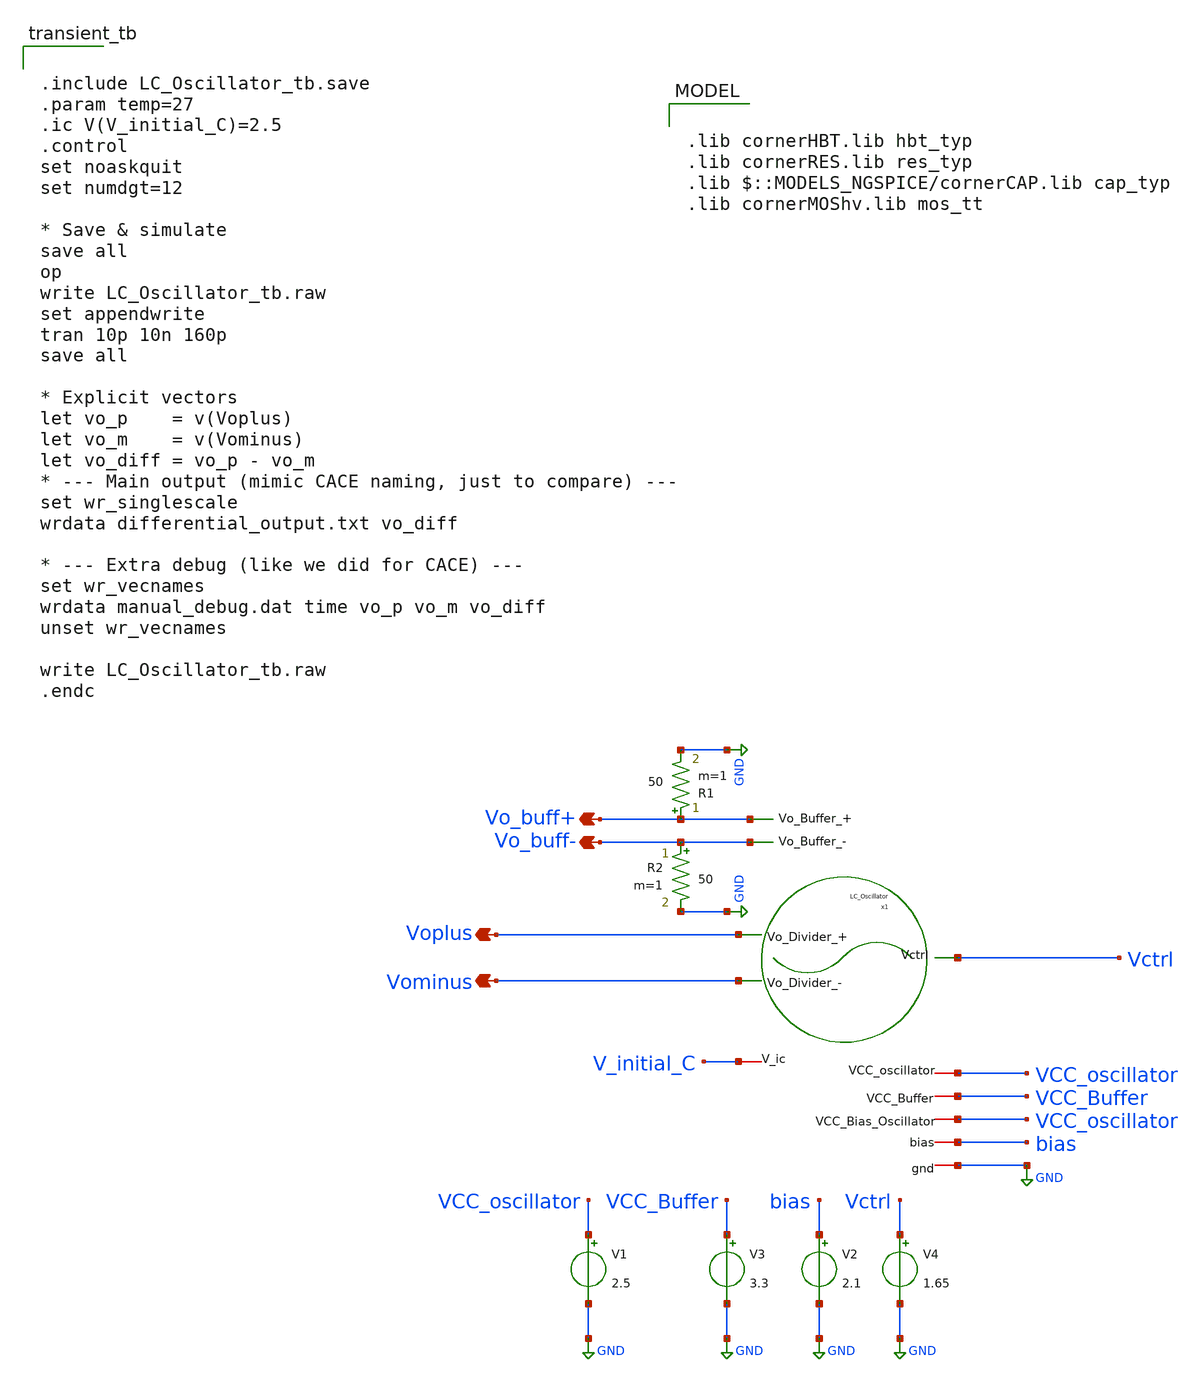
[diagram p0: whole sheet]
** sch_path: modules/module_4_type_2_PLL/LC_Oscillator/testbench/LC_Oscillator_tb.sch
**.subckt LC_Oscillator_tb Voplus Vominus Vo_buff+ Vo_buff-
*.opin Voplus
*.opin Vominus
*.opin Vo_buff+
*.opin Vo_buff-
V1 VCC_oscillator GND 2.5
x1 Voplus VCC_oscillator GND Vominus Vctrl bias VCC_Buffer VCC_oscillator Vo_buff- Vo_buff+
+ V_initial_C LC_Oscillator
V2 bias GND 2.1
V3 VCC_Buffer GND 3.3
R1 Vo_buff+ GND 50 m=1
R2 Vo_buff- GND 50 m=1
V4 Vctrl GND 1.65
**** begin user architecture code


.include LC_Oscillator_tb.save
.param temp=27
.ic V(V_initial_C)=2.5
.control
set noaskquit
set numdgt=12

* Save & simulate
save all
op
write LC_Oscillator_tb.raw
set appendwrite
tran 10p 10n 160p
save all

* Explicit vectors
let vo_p    = v(Voplus)
let vo_m    = v(Vominus)
let vo_diff = vo_p - vo_m
* --- Main output (mimic CACE naming, just to compare) ---
set wr_singlescale
wrdata differential_output.txt vo_diff

* --- Extra debug (like we did for CACE) ---
set wr_vecnames
wrdata manual_debug.dat time vo_p vo_m vo_diff
unset wr_vecnames

write LC_Oscillator_tb.raw
.endc



.lib cornerHBT.lib hbt_typ
.lib cornerRES.lib res_typ
.lib $::MODELS_NGSPICE/cornerCAP.lib cap_typ
.lib cornerMOShv.lib mos_tt

**** end user architecture code
**.ends

* expanding   symbol:  LC_Oscillator.sym # of pins=11
** sym_path: modules/module_4_type_2_PLL/LC_Oscillator/xschem/LC_Oscillator.sym
** sch_path: modules/module_4_type_2_PLL/LC_Oscillator/xschem/LC_Oscillator.sch
.subckt LC_Oscillator Vo_Divider_+ VCC_oscillator gnd Vo_Divider_- Vctrl bias VCC_Buffer
+ VCC_Bias_Oscillator Vo_Buffer_- Vo_Buffer_+ V_ic
*.iopin VCC_oscillator
*.iopin VCC_Bias_Oscillator
*.opin Vo_Buffer_-
*.iopin gnd
*.ipin Vctrl
*.iopin VCC_Buffer
*.opin Vo_Buffer_+
*.opin Vo_Divider_-
*.opin Vo_Divider_+
*.iopin bias
*.iopin V_ic
XC5 V_ic net5 gnd cap_rfcmim w=7.24e-6 l=7.24e-6 wfeed=5.0e-6 m=1 mm_ok=1
XQ2 net1 net9 net11 sub! npn13G2 Nx=1 mm_ok=1
XC2 V_ic net10 gnd cap_rfcmim w=9.065e-6 l=9.065e-6 wfeed=3.0e-6 m=1 mm_ok=1
XQ3 net3 net10 net11 sub! npn13G2 Nx=3 mm_ok=1
L5 VCC_oscillator net3 62.5p m=1
L6 net3 V_tank_- 62.5p m=1
XC13 net5 Vctrl net6 sub! sg13_hv_svaricap w=9.74u l=0.8u Nx=10 mm_ok=1
XC14 net7 Vctrl net8 sub! sg13_hv_svaricap w=9.74u l=0.8u Nx=10 mm_ok=1
XC15 net9 Vo- gnd cap_rfcmim w=18.195e-6 l=18.195e-6 wfeed=3.0e-6 m=1 mm_ok=1
XC16 Vo- VCC_oscillator gnd cap_rfcmim w=18.195e-6 l=18.195e-6 wfeed=3.0e-6 m=1 mm_ok=1
XR1 net9 bias sub! rppd w=820e-9 l=1e-6 m=4 b=0 mm_ok=1
XC17 net10 Vo+ gnd cap_rfcmim w=18.195e-6 l=18.195e-6 wfeed=3.0e-6 m=1 mm_ok=1
XC18 Vo+ VCC_oscillator gnd cap_rfcmim w=18.195e-6 l=18.195e-6 wfeed=3.0e-6 m=1 mm_ok=1
XR2 net10 bias sub! rppd w=820e-9 l=1e-6 m=4 b=0 mm_ok=1
L7 net11 net12 50p m=1
XC19 net11 gnd gnd cap_rfcmim w=7.2e-6 l=7.2e-6 wfeed=3.0e-6 m=1 mm_ok=1
XQ5 net12 net15 net13 sub! npn13G2 Nx=4 mm_ok=1
XQ6 net15 net15 net14 sub! npn13G2 Nx=1 mm_ok=1
XR4 net13 gnd sub! rppd w=1.3e-6 l=4.55e-6 m=12 b=0 mm_ok=1
XR5 net14 gnd sub! rppd w=1.3e-6 l=4.55e-6 m=4 b=0 mm_ok=1
XR6 VCC_Bias_Oscillator net15 sub! rppd w=1.3e-6 l=4.55e-6 m=4 b=0 mm_ok=1
XC20 net12 gnd gnd cap_rfcmim w=9.1e-6 l=9.1e-6 wfeed=3.0e-6 m=1 mm_ok=1
XC21 V_ic net2 gnd cap_rfcmim w=11.485e-6 l=11.485e-6 wfeed=3.0e-6 m=1 mm_ok=1
XC1 net2 net7 gnd cap_rfcmim w=11.485e-6 l=11.485e-6 wfeed=3.0e-6 m=1 mm_ok=1
XC3 V_tank_- net9 gnd cap_rfcmim w=9.065e-6 l=9.065e-6 wfeed=3.0e-6 m=1 mm_ok=1
XC7 V_tank_- net4 gnd cap_rfcmim w=11.485e-6 l=11.485e-6 wfeed=3.0e-6 m=1 mm_ok=1
XC8 net4 net8 gnd cap_rfcmim w=11.485e-6 l=11.485e-6 wfeed=3.0e-6 m=1 mm_ok=1
XC6 V_tank_- net6 gnd cap_rfcmim w=7.24e-6 l=7.24e-6 wfeed=5.0e-6 m=1 mm_ok=1
L1 net1 V_ic 62.5p m=1
L2 VCC_oscillator net1 62.5p m=1
XQ4 VCC_Buffer Vo- Vo_Buffer_- sub! npn13G2 Nx=6 mm_ok=1
XR3 Vo_Buffer_- gnd sub! rppd w=2e-6 l=10.955e-6 m=4 b=0 mm_ok=1
XR8 net16 Vo- sub! rppd w=0.5e-6 l=1.675e-6 m=2 b=0 mm_ok=1
XR9 VCC_Buffer net16 sub! rppd w=0.5e-6 l=1.675e-6 m=2 b=0 mm_ok=1
XR10 Vo- net19 sub! rppd w=0.5e-6 l=1.675e-6 m=2 b=0 mm_ok=1
XR11 net19 net18 sub! rppd w=0.5e-6 l=1.675e-6 m=2 b=0 mm_ok=1
XR12 net18 net17 sub! rppd w=0.5e-6 l=1.675e-6 m=2 b=0 mm_ok=1
XR13 net17 gnd sub! rppd w=0.5e-6 l=1.675e-6 m=2 b=0 mm_ok=1
XQ7 VCC_Buffer Vo+ Vo_Buffer_+ sub! npn13G2 Nx=6 mm_ok=1
XR14 Vo_Buffer_+ gnd sub! rppd w=2e-6 l=10.955e-6 m=4 b=0 mm_ok=1
XR16 net20 Vo+ sub! rppd w=0.5e-6 l=1.675e-6 m=2 b=0 mm_ok=1
XR17 VCC_Buffer net20 sub! rppd w=0.5e-6 l=1.675e-6 m=2 b=0 mm_ok=1
XR18 Vo+ net23 sub! rppd w=0.5e-6 l=1.675e-6 m=2 b=0 mm_ok=1
XR19 net23 net22 sub! rppd w=0.5e-6 l=1.675e-6 m=2 b=0 mm_ok=1
XR20 net22 net21 sub! rppd w=0.5e-6 l=1.675e-6 m=2 b=0 mm_ok=1
XR21 net21 gnd sub! rppd w=0.5e-6 l=1.675e-6 m=2 b=0 mm_ok=1
XQ8 VCC_Buffer Vo- Vo_Divider_- sub! npn13G2 Nx=6 mm_ok=1
XR7 Vo_Divider_- gnd sub! rppd w=2e-6 l=10.955e-6 m=4 b=0 mm_ok=1
XR15 net24 Vo- sub! rppd w=0.5e-6 l=1.675e-6 m=2 b=0 mm_ok=1
XR22 VCC_Buffer net24 sub! rppd w=0.5e-6 l=1.675e-6 m=2 b=0 mm_ok=1
XQ9 VCC_Buffer Vo+ Vo_Divider_+ sub! npn13G2 Nx=6 mm_ok=1
XR27 Vo_Divider_+ gnd sub! rppd w=2e-6 l=10.955e-6 m=4 b=0 mm_ok=1
XR28 net25 Vo+ sub! rppd w=0.5e-6 l=1.675e-6 m=2 b=0 mm_ok=1
XR29 VCC_Buffer net25 sub! rppd w=0.5e-6 l=1.675e-6 m=2 b=0 mm_ok=1
XC9 Vo- gnd gnd cap_rfcmim w=18.195e-6 l=18.195e-6 wfeed=3.0e-6 m=1 mm_ok=1
XC10 Vo+ gnd gnd cap_rfcmim w=18.195e-6 l=18.195e-6 wfeed=3.0e-6 m=1 mm_ok=1
XR23 gnd sub! ptap1 R=262.8 w=0.78e-6 l=0.78e-6
XR24 gnd sub! ptap1 R=262.8 w=0.78e-6 l=0.78e-6
XR25 gnd sub! ptap1 R=262.8 w=0.78e-6 l=0.78e-6
XR26 gnd sub! ptap1 R=262.8 w=0.78e-6 l=0.78e-6
XR30 gnd sub! ptap1 R=262.8 w=0.78e-6 l=0.78e-6
XR31 gnd sub! ptap1 R=262.8 w=0.78e-6 l=0.78e-6
.ends

.GLOBAL GND
.end
